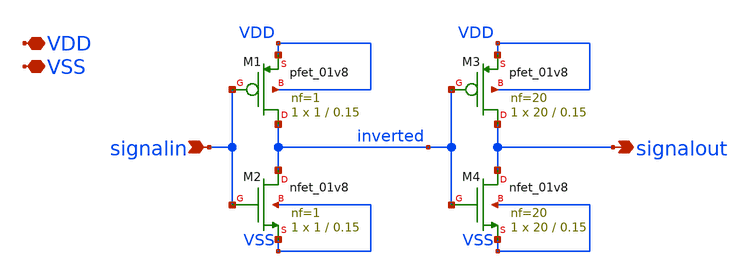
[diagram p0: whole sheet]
** sch_path: xschem/doubleinverter.sch
**.subckt doubleinverter VDD VSS signalin signalout
*.iopin VDD
*.iopin VSS
*.ipin signalin
*.opin signalout
XM1 inverted signalin VDD VDD sky130_fd_pr__pfet_01v8 L=0.15 W=1 nf=1 ad='int((nf+1)/2) * W/nf * 0.29'
+ as='int((nf+2)/2) * W/nf * 0.29' pd='2*int((nf+1)/2) * (W/nf + 0.29)' ps='2*int((nf+2)/2) * (W/nf + 0.29)'
+ nrd='0.29 / W' nrs='0.29 / W' sa=0 sb=0 sd=0 mult=1 m=1
XM2 inverted signalin VSS VSS sky130_fd_pr__nfet_01v8 L=0.15 W=1 nf=1 ad='int((nf+1)/2) * W/nf * 0.29'
+ as='int((nf+2)/2) * W/nf * 0.29' pd='2*int((nf+1)/2) * (W/nf + 0.29)' ps='2*int((nf+2)/2) * (W/nf + 0.29)'
+ nrd='0.29 / W' nrs='0.29 / W' sa=0 sb=0 sd=0 mult=1 m=1
XM3 signalout inverted VDD VDD sky130_fd_pr__pfet_01v8 L=0.15 W=20 nf=20 ad='int((nf+1)/2) * W/nf * 0.29'
+ as='int((nf+2)/2) * W/nf * 0.29' pd='2*int((nf+1)/2) * (W/nf + 0.29)' ps='2*int((nf+2)/2) * (W/nf + 0.29)'
+ nrd='0.29 / W' nrs='0.29 / W' sa=0 sb=0 sd=0 mult=1 m=1
XM4 signalout inverted VSS VSS sky130_fd_pr__nfet_01v8 L=0.15 W=20 nf=20 ad='int((nf+1)/2) * W/nf * 0.29'
+ as='int((nf+2)/2) * W/nf * 0.29' pd='2*int((nf+1)/2) * (W/nf + 0.29)' ps='2*int((nf+2)/2) * (W/nf + 0.29)'
+ nrd='0.29 / W' nrs='0.29 / W' sa=0 sb=0 sd=0 mult=1 m=1
**.ends
.end
